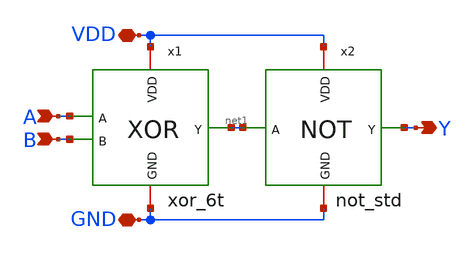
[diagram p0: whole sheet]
** sch_path: parity_ceker/schematic/xnor_6t_buf.sch
**.subckt xnor_6t_buf A B Y VDD GND
*.ipin A
*.ipin B
*.opin Y
*.iopin VDD
*.iopin GND
x1 VDD net1 A B GND xor_6t
x2 VDD net1 Y GND not_std
**.ends
.end
